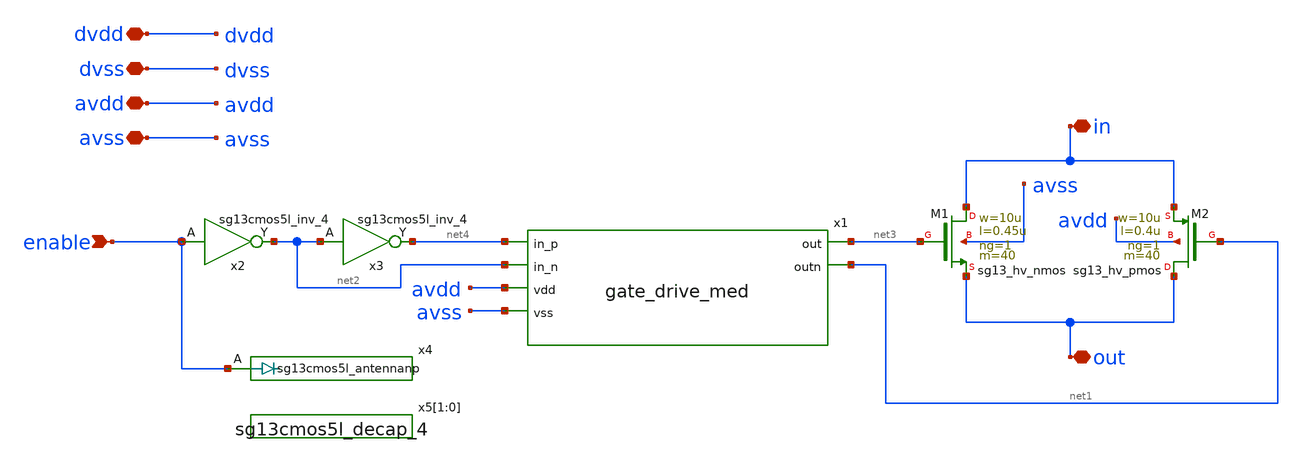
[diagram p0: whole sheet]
** sch_path: macros/ocd_analog_switches/schematic/xschem/analog_switch_med.sch
**.subckt analog_switch_med in out enable dvdd dvss avdd avss
*.iopin in
*.iopin out
*.ipin enable
*.iopin dvdd
*.iopin dvss
*.iopin avdd
*.iopin avss
XM1 in net3 out avss sg13_hv_nmos w=10u l=0.45u ng=1 m=40 mm_ok=1
XM2 out net1 in avdd sg13_hv_pmos w=10u l=0.4u ng=1 m=40 mm_ok=1
x2 net2 enable dvdd dvss sg13cmos5l_inv_4
x3 net4 net2 dvdd dvss sg13cmos5l_inv_4
x4 enable dvdd dvss sg13cmos5l_antennanp
x5[1] dvdd dvss sg13cmos5l_decap_4
x5[0] dvdd dvss sg13cmos5l_decap_4
x1 net2 net4 net3 avdd avss net1 gate_drive_med
**.ends

* expanding   symbol:  gate_drive_med.sym # of pins=6
** sym_path: macros/ocd_analog_switches/schematic/xschem/gate_drive_med.sym
** sch_path: macros/ocd_analog_switches/schematic/xschem/gate_drive_med.sch
.subckt gate_drive_med in_n in_p out vdd vss outn
*.ipin in_n
*.ipin in_p
*.ipin vdd
*.ipin vss
*.opin out
*.opin outn
XM1 net1 in_p vss vss sg13_hv_nmos w=2u l=0.5u ng=1 m=1 mm_ok=1
XM2 net1 S1_P vdd vdd sg13_hv_pmos w=0.5u l=0.5u ng=1 m=1 mm_ok=1
XM3 S1_P in_n vss vss sg13_hv_nmos w=2u l=0.5u ng=1 m=1 mm_ok=1
XM4 S1_P net1 vdd vdd sg13_hv_pmos w=0.5u l=0.5u ng=1 m=1 mm_ok=1
XM5 S2_N S1_P vdd vdd sg13_hv_pmos w=10u l=0.5u ng=1 m=2 mm_ok=1
XM6 S2_N S1_P vss vss sg13_hv_nmos w=5u l=0.5u ng=1 m=2 mm_ok=1
XM7 S3_P S2_N vdd vdd sg13_hv_pmos w=10u l=0.5u ng=1 m=6 mm_ok=1
XM8 S3_P S2_N vss vss sg13_hv_nmos w=5u l=0.5u ng=1 m=6 mm_ok=1
XM9 outn S3_P vdd vdd sg13_hv_pmos w=10u l=0.5u ng=1 m=16 mm_ok=1
XM10 outn S3_P vss vss sg13_hv_nmos w=5u l=0.5u ng=1 m=16 mm_ok=1
XM11 out outn vdd vdd sg13_hv_pmos w=10u l=0.5u ng=1 m=16 mm_ok=1
XM12 out outn vss vss sg13_hv_nmos w=5u l=0.5u ng=1 m=16 mm_ok=1
.ends

.end
